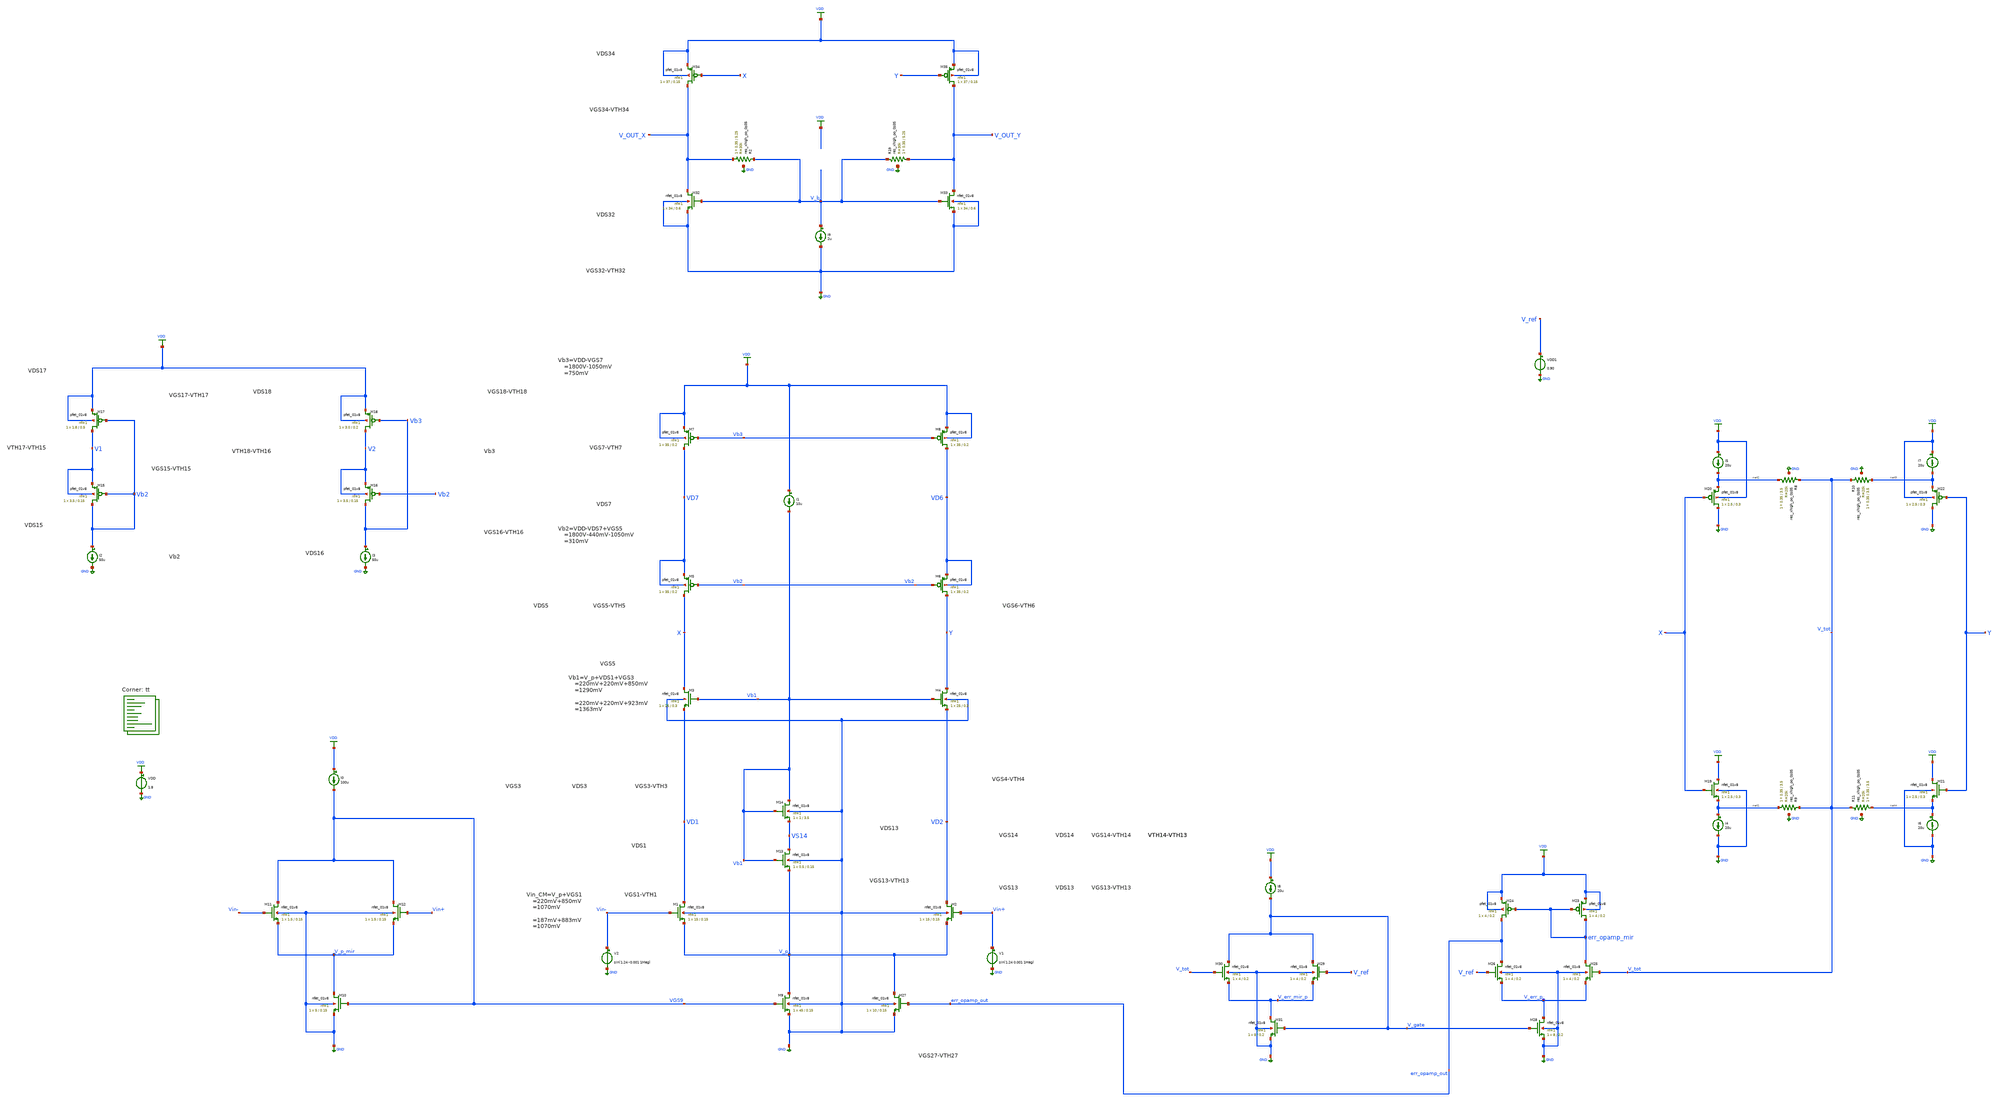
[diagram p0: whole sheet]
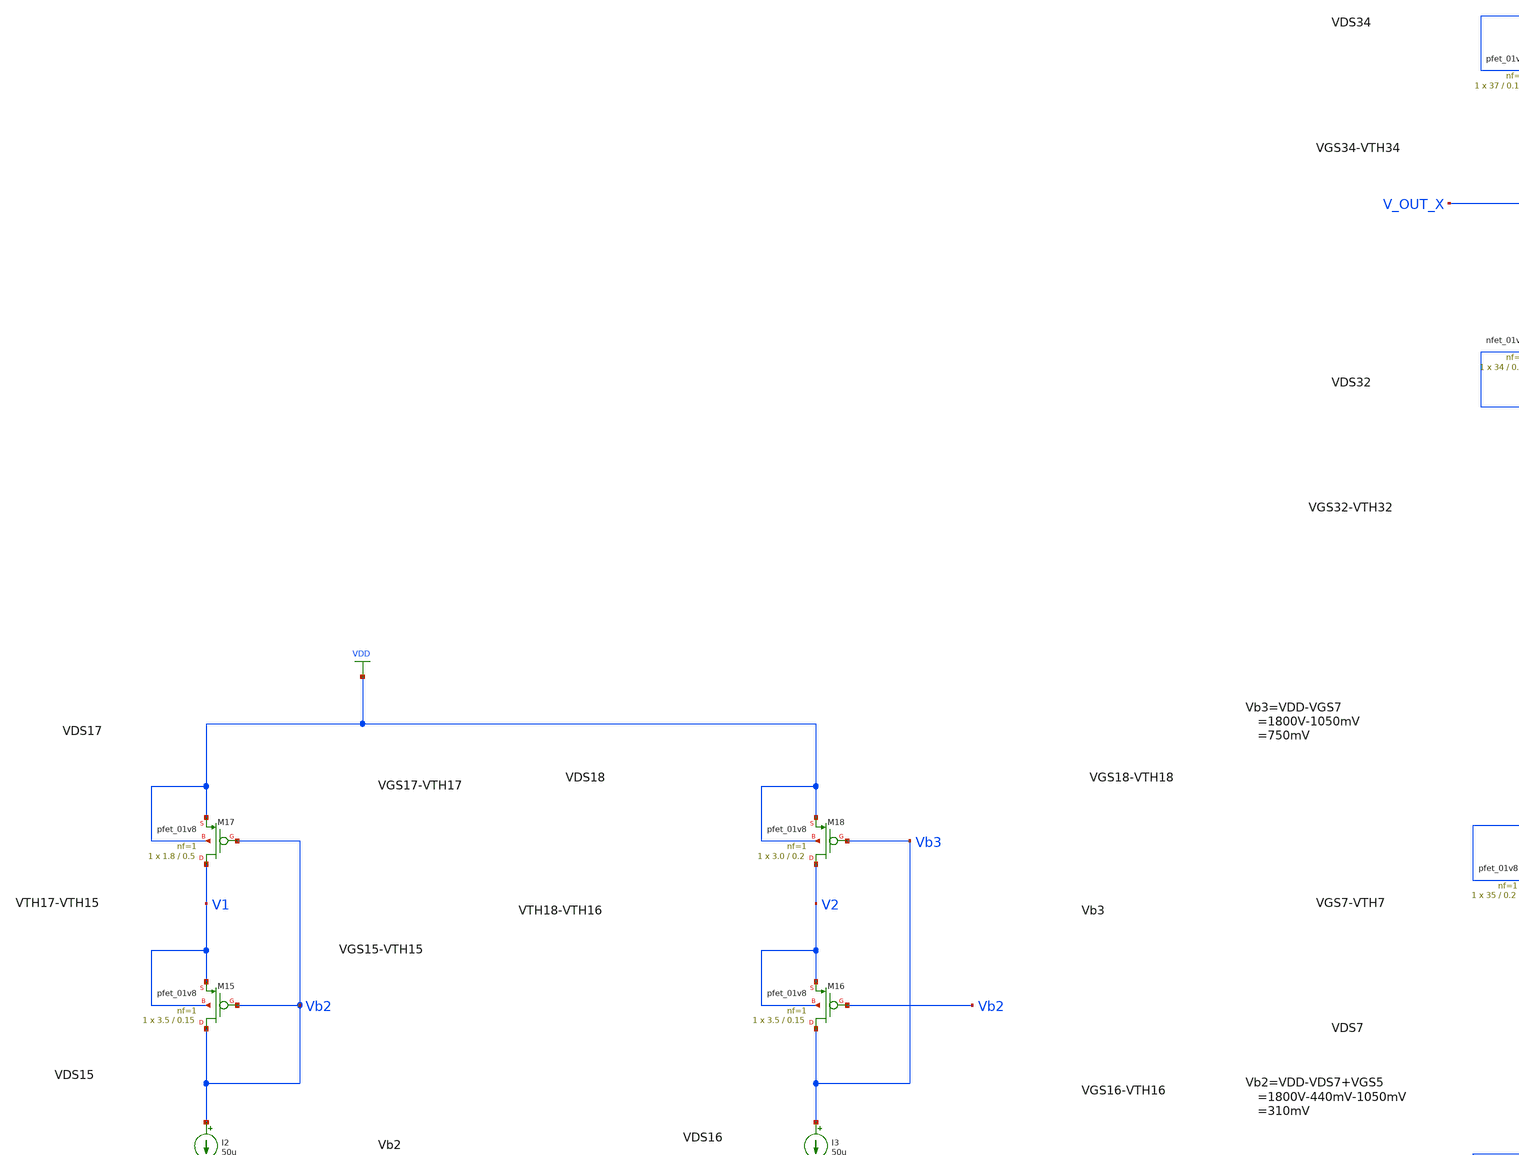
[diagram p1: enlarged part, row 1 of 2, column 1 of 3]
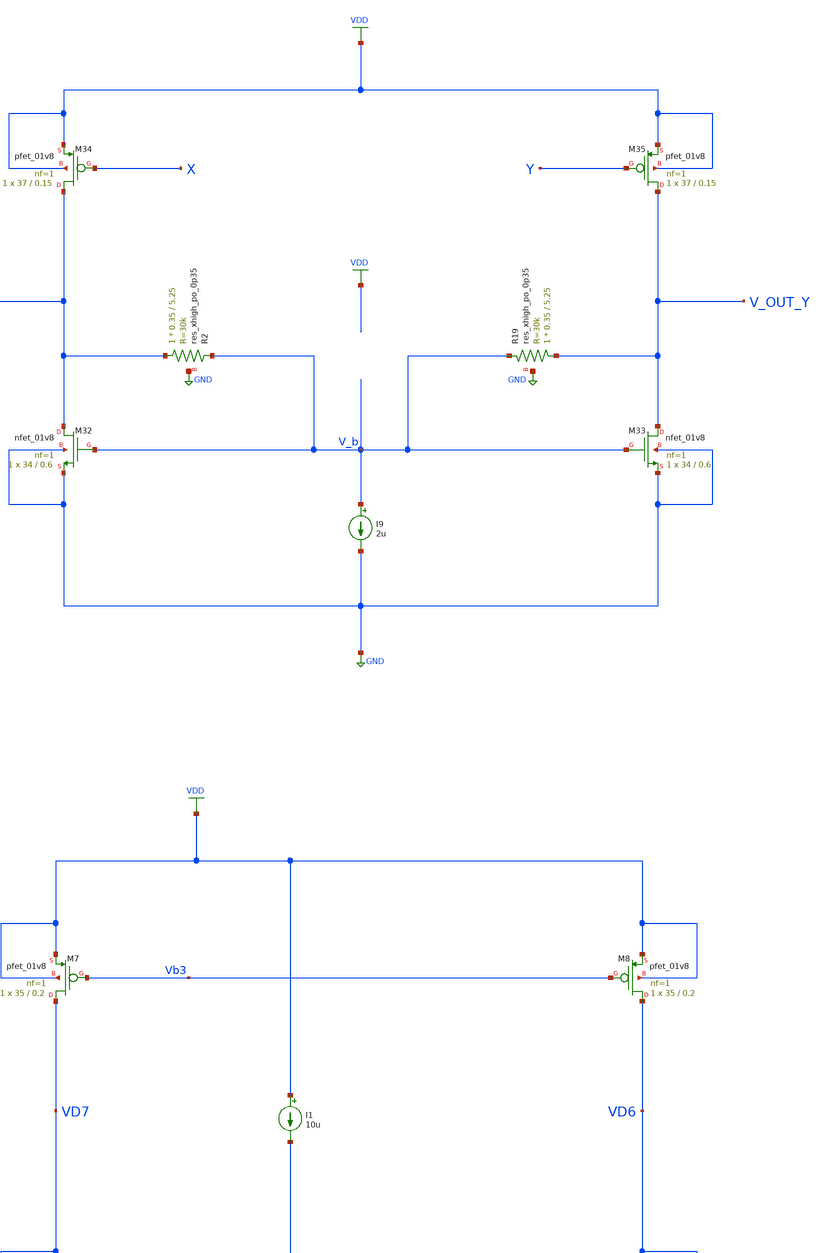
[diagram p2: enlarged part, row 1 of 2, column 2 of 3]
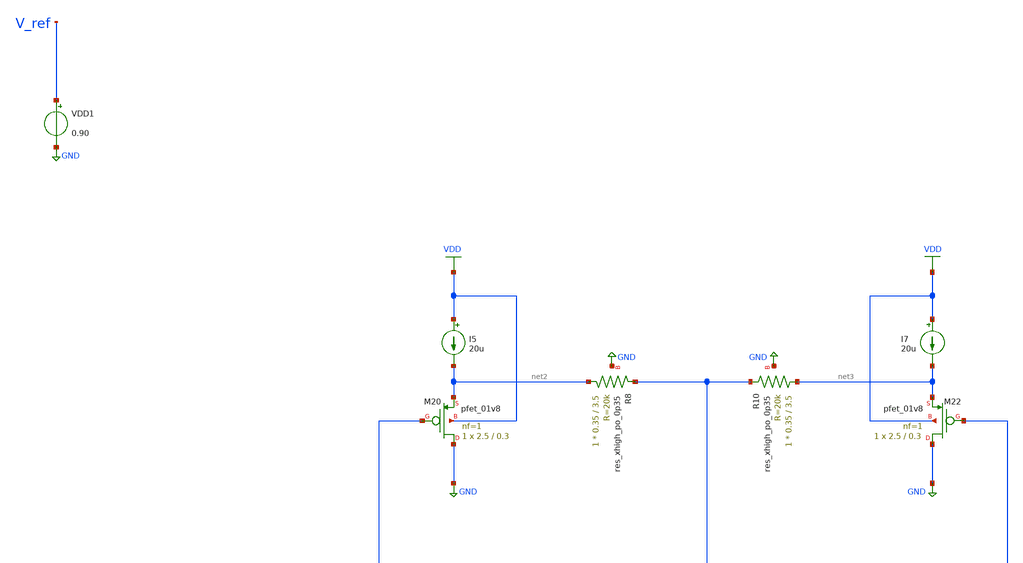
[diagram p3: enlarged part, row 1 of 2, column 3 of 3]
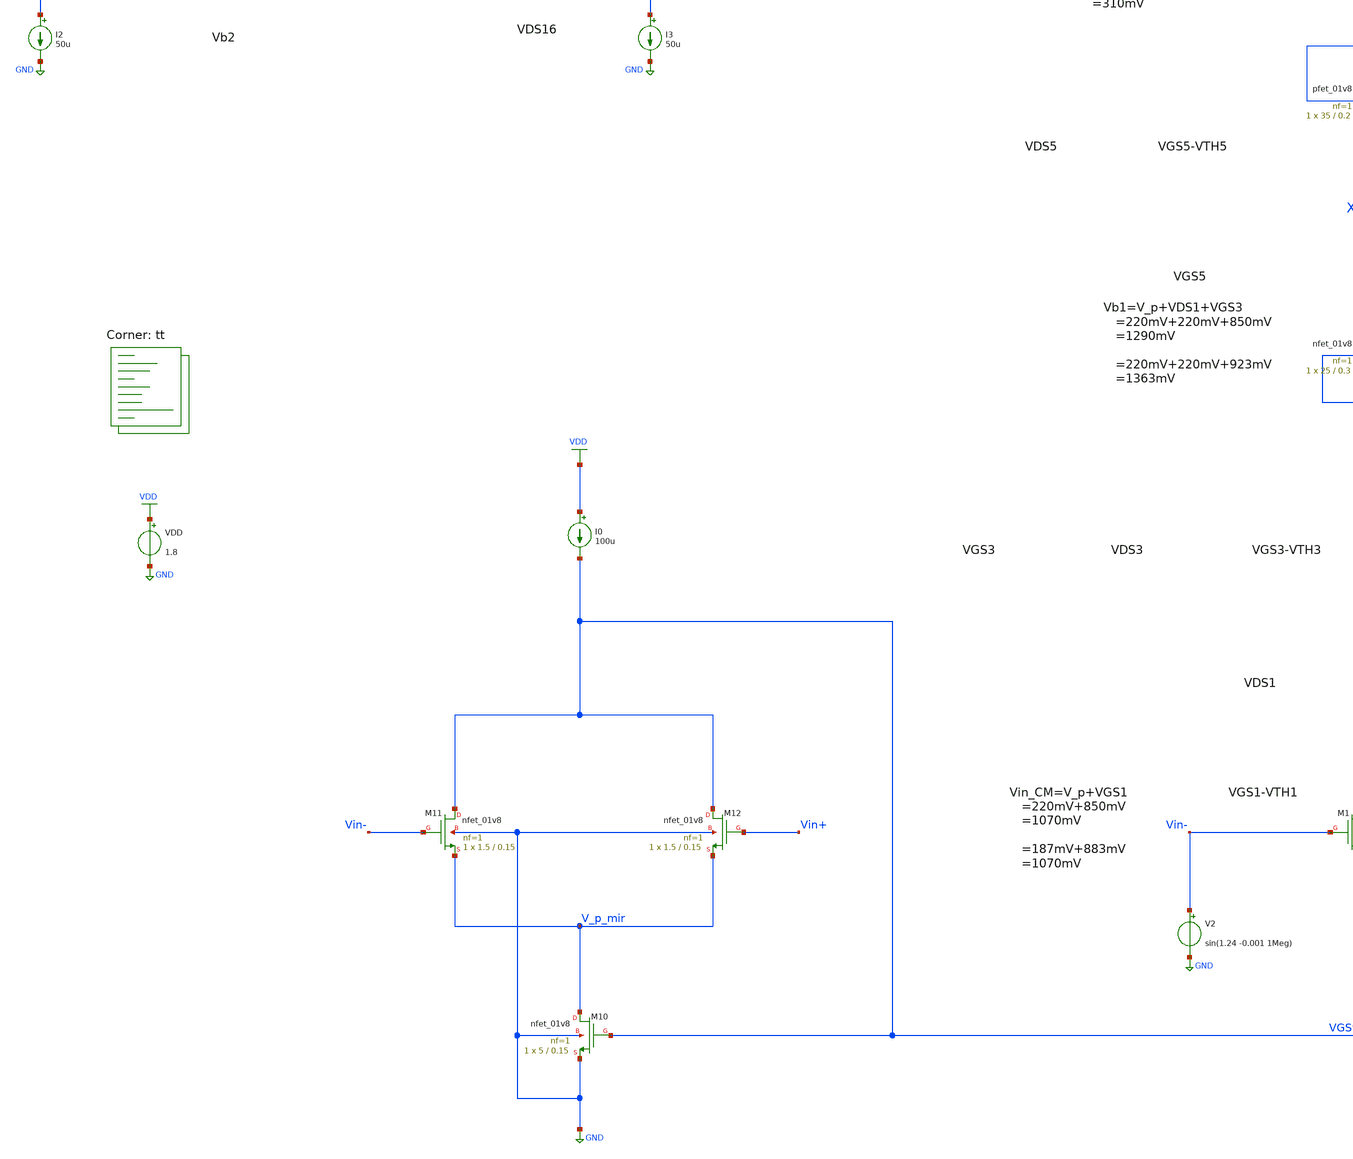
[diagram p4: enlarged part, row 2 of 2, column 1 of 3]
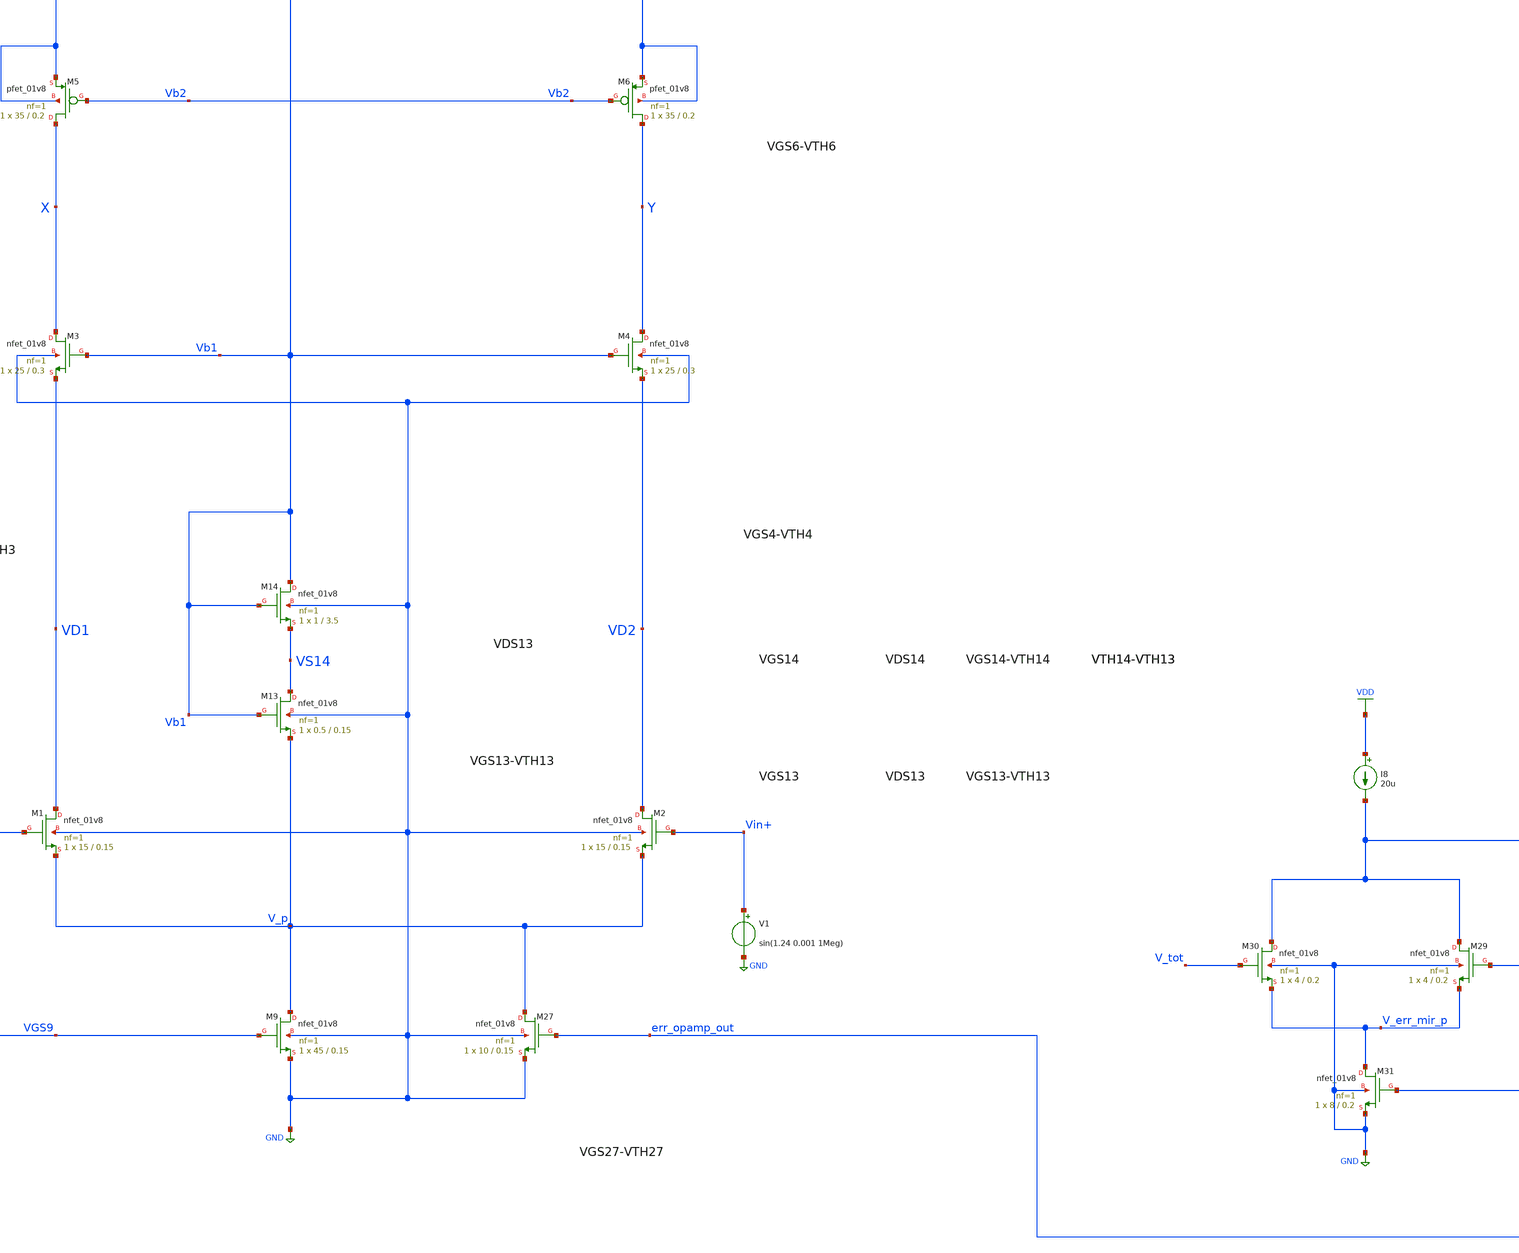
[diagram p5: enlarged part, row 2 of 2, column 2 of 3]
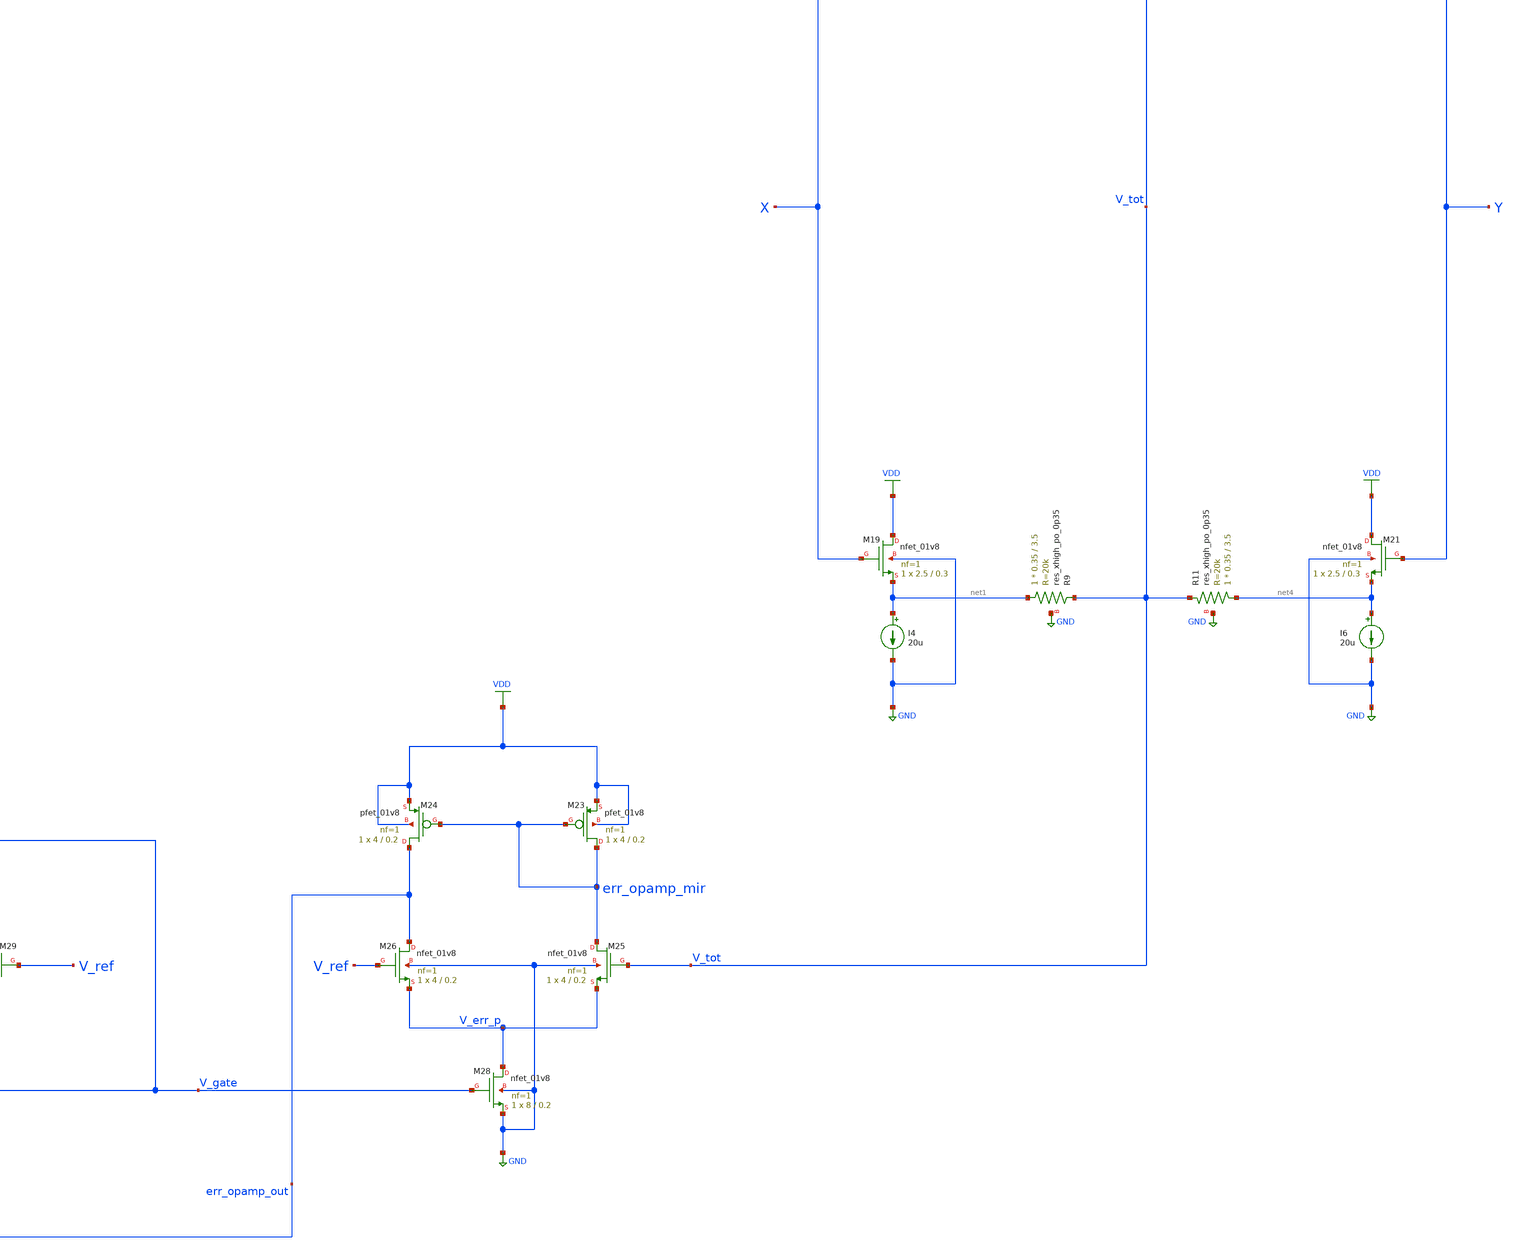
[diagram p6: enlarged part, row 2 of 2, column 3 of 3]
** sch_path: projects/opamp/xschem_ngspice/tb_opamp_1st_stage_3.sch
**.subckt tb_opamp_1st_stage_3
VDD VDD GND 1.8
XM1 VD1 Vin- V_p GND sky130_fd_pr__nfet_01v8 L=0.15 W=15 nf=1 ad='int((nf+1)/2) * W/nf * 0.29' as='int((nf+2)/2) * W/nf * 0.29'
+ pd='2*int((nf+1)/2) * (W/nf + 0.29)' ps='2*int((nf+2)/2) * (W/nf + 0.29)' nrd='0.29 / W' nrs='0.29 / W'
+ sa=0 sb=0 sd=0 mult=1 m=1
XM2 VD2 Vin+ V_p GND sky130_fd_pr__nfet_01v8 L=0.15 W=15 nf=1 ad='int((nf+1)/2) * W/nf * 0.29' as='int((nf+2)/2) * W/nf * 0.29'
+ pd='2*int((nf+1)/2) * (W/nf + 0.29)' ps='2*int((nf+2)/2) * (W/nf + 0.29)' nrd='0.29 / W' nrs='0.29 / W'
+ sa=0 sb=0 sd=0 mult=1 m=1
XM3 X Vb1 VD1 GND sky130_fd_pr__nfet_01v8 L=0.3 W=25 nf=1 ad='int((nf+1)/2) * W/nf * 0.29' as='int((nf+2)/2) * W/nf * 0.29'
+ pd='2*int((nf+1)/2) * (W/nf + 0.29)' ps='2*int((nf+2)/2) * (W/nf + 0.29)' nrd='0.29 / W' nrs='0.29 / W'
+ sa=0 sb=0 sd=0 mult=1 m=1
XM4 Y Vb1 VD2 GND sky130_fd_pr__nfet_01v8 L=0.3 W=25 nf=1 ad='int((nf+1)/2) * W/nf * 0.29' as='int((nf+2)/2) * W/nf * 0.29'
+ pd='2*int((nf+1)/2) * (W/nf + 0.29)' ps='2*int((nf+2)/2) * (W/nf + 0.29)' nrd='0.29 / W' nrs='0.29 / W'
+ sa=0 sb=0 sd=0 mult=1 m=1
XM5 X Vb2 VD7 VD7 sky130_fd_pr__pfet_01v8 L=0.2 W=35 nf=1 ad='int((nf+1)/2) * W/nf * 0.29' as='int((nf+2)/2) * W/nf * 0.29'
+ pd='2*int((nf+1)/2) * (W/nf + 0.29)' ps='2*int((nf+2)/2) * (W/nf + 0.29)' nrd='0.29 / W' nrs='0.29 / W'
+ sa=0 sb=0 sd=0 mult=1 m=1
XM6 Y Vb2 VD6 VD6 sky130_fd_pr__pfet_01v8 L=0.2 W=35 nf=1 ad='int((nf+1)/2) * W/nf * 0.29' as='int((nf+2)/2) * W/nf * 0.29'
+ pd='2*int((nf+1)/2) * (W/nf + 0.29)' ps='2*int((nf+2)/2) * (W/nf + 0.29)' nrd='0.29 / W' nrs='0.29 / W'
+ sa=0 sb=0 sd=0 mult=1 m=1
XM7 VD7 Vb3 VDD VDD sky130_fd_pr__pfet_01v8 L=0.2 W=35 nf=1 ad='int((nf+1)/2) * W/nf * 0.29' as='int((nf+2)/2) * W/nf * 0.29'
+ pd='2*int((nf+1)/2) * (W/nf + 0.29)' ps='2*int((nf+2)/2) * (W/nf + 0.29)' nrd='0.29 / W' nrs='0.29 / W'
+ sa=0 sb=0 sd=0 mult=1 m=1
XM8 VD6 Vb3 VDD VDD sky130_fd_pr__pfet_01v8 L=0.2 W=35 nf=1 ad='int((nf+1)/2) * W/nf * 0.29' as='int((nf+2)/2) * W/nf * 0.29'
+ pd='2*int((nf+1)/2) * (W/nf + 0.29)' ps='2*int((nf+2)/2) * (W/nf + 0.29)' nrd='0.29 / W' nrs='0.29 / W'
+ sa=0 sb=0 sd=0 mult=1 m=1
XM9 V_p VGS9 GND GND sky130_fd_pr__nfet_01v8 L=0.15 W=45 nf=1 ad='int((nf+1)/2) * W/nf * 0.29' as='int((nf+2)/2) * W/nf * 0.29'
+ pd='2*int((nf+1)/2) * (W/nf + 0.29)' ps='2*int((nf+2)/2) * (W/nf + 0.29)' nrd='0.29 / W' nrs='0.29 / W'
+ sa=0 sb=0 sd=0 mult=1 m=1
XM10 V_p_mir VGS9 GND GND sky130_fd_pr__nfet_01v8 L=0.15 W=5 nf=1 ad='int((nf+1)/2) * W/nf * 0.29' as='int((nf+2)/2) * W/nf * 0.29'
+ pd='2*int((nf+1)/2) * (W/nf + 0.29)' ps='2*int((nf+2)/2) * (W/nf + 0.29)' nrd='0.29 / W' nrs='0.29 / W'
+ sa=0 sb=0 sd=0 mult=1 m=1
I0 VDD VGS9 100u
XM11 VGS9 Vin- V_p_mir GND sky130_fd_pr__nfet_01v8 L=0.15 W=1.5 nf=1 ad='int((nf+1)/2) * W/nf * 0.29'
+ as='int((nf+2)/2) * W/nf * 0.29' pd='2*int((nf+1)/2) * (W/nf + 0.29)' ps='2*int((nf+2)/2) * (W/nf + 0.29)'
+ nrd='0.29 / W' nrs='0.29 / W' sa=0 sb=0 sd=0 mult=1 m=1
XM12 VGS9 Vin+ V_p_mir GND sky130_fd_pr__nfet_01v8 L=0.15 W=1.5 nf=1 ad='int((nf+1)/2) * W/nf * 0.29'
+ as='int((nf+2)/2) * W/nf * 0.29' pd='2*int((nf+1)/2) * (W/nf + 0.29)' ps='2*int((nf+2)/2) * (W/nf + 0.29)'
+ nrd='0.29 / W' nrs='0.29 / W' sa=0 sb=0 sd=0 mult=1 m=1
XM13 VS14 Vb1 V_p GND sky130_fd_pr__nfet_01v8 L=0.15 W=0.5 nf=1 ad='int((nf+1)/2) * W/nf * 0.29' as='int((nf+2)/2) * W/nf * 0.29'
+ pd='2*int((nf+1)/2) * (W/nf + 0.29)' ps='2*int((nf+2)/2) * (W/nf + 0.29)' nrd='0.29 / W' nrs='0.29 / W'
+ sa=0 sb=0 sd=0 mult=1 m=1
XM14 Vb1 Vb1 VS14 GND sky130_fd_pr__nfet_01v8 L=3.5 W=1 nf=1 ad='int((nf+1)/2) * W/nf * 0.29' as='int((nf+2)/2) * W/nf * 0.29'
+ pd='2*int((nf+1)/2) * (W/nf + 0.29)' ps='2*int((nf+2)/2) * (W/nf + 0.29)' nrd='0.29 / W' nrs='0.29 / W'
+ sa=0 sb=0 sd=0 mult=1 m=1
I1 VDD Vb1 10u
XM15 Vb2 Vb2 V1 V1 sky130_fd_pr__pfet_01v8 L=0.15 W=3.5 nf=1 ad='int((nf+1)/2) * W/nf * 0.29' as='int((nf+2)/2) * W/nf * 0.29'
+ pd='2*int((nf+1)/2) * (W/nf + 0.29)' ps='2*int((nf+2)/2) * (W/nf + 0.29)' nrd='0.29 / W' nrs='0.29 / W'
+ sa=0 sb=0 sd=0 mult=1 m=1
XM16 Vb3 Vb2 V2 V2 sky130_fd_pr__pfet_01v8 L=0.15 W=3.5 nf=1 ad='int((nf+1)/2) * W/nf * 0.29' as='int((nf+2)/2) * W/nf * 0.29'
+ pd='2*int((nf+1)/2) * (W/nf + 0.29)' ps='2*int((nf+2)/2) * (W/nf + 0.29)' nrd='0.29 / W' nrs='0.29 / W'
+ sa=0 sb=0 sd=0 mult=1 m=1
XM17 V1 Vb2 VDD VDD sky130_fd_pr__pfet_01v8 L=0.5 W=1.8 nf=1 ad='int((nf+1)/2) * W/nf * 0.29' as='int((nf+2)/2) * W/nf * 0.29'
+ pd='2*int((nf+1)/2) * (W/nf + 0.29)' ps='2*int((nf+2)/2) * (W/nf + 0.29)' nrd='0.29 / W' nrs='0.29 / W'
+ sa=0 sb=0 sd=0 mult=1 m=1
XM18 V2 Vb3 VDD VDD sky130_fd_pr__pfet_01v8 L=0.2 W=3.0 nf=1 ad='int((nf+1)/2) * W/nf * 0.29' as='int((nf+2)/2) * W/nf * 0.29'
+ pd='2*int((nf+1)/2) * (W/nf + 0.29)' ps='2*int((nf+2)/2) * (W/nf + 0.29)' nrd='0.29 / W' nrs='0.29 / W'
+ sa=0 sb=0 sd=0 mult=1 m=1
I2 Vb2 GND 50u
I3 Vb3 GND 50u
XM19 VDD X net1 GND sky130_fd_pr__nfet_01v8 L=0.3 W=2.5 nf=1 ad='int((nf+1)/2) * W/nf * 0.29' as='int((nf+2)/2) * W/nf * 0.29'
+ pd='2*int((nf+1)/2) * (W/nf + 0.29)' ps='2*int((nf+2)/2) * (W/nf + 0.29)' nrd='0.29 / W' nrs='0.29 / W'
+ sa=0 sb=0 sd=0 mult=1 m=1
XM20 GND X net2 VDD sky130_fd_pr__pfet_01v8 L=0.3 W=2.5 nf=1 ad='int((nf+1)/2) * W/nf * 0.29' as='int((nf+2)/2) * W/nf * 0.29'
+ pd='2*int((nf+1)/2) * (W/nf + 0.29)' ps='2*int((nf+2)/2) * (W/nf + 0.29)' nrd='0.29 / W' nrs='0.29 / W'
+ sa=0 sb=0 sd=0 mult=1 m=1
I4 net1 GND 20u
I5 VDD net2 20u
XR8 net2 V_tot GND sky130_fd_pr__res_xhigh_po_0p35 L=3.5 mult=1 m=1
XR9 net1 V_tot GND sky130_fd_pr__res_xhigh_po_0p35 L=3.5 mult=1 m=1
XR10 net3 V_tot GND sky130_fd_pr__res_xhigh_po_0p35 L=3.5 mult=1 m=1
XR11 net4 V_tot GND sky130_fd_pr__res_xhigh_po_0p35 L=3.5 mult=1 m=1
XM21 VDD Y net4 GND sky130_fd_pr__nfet_01v8 L=0.3 W=2.5 nf=1 ad='int((nf+1)/2) * W/nf * 0.29' as='int((nf+2)/2) * W/nf * 0.29'
+ pd='2*int((nf+1)/2) * (W/nf + 0.29)' ps='2*int((nf+2)/2) * (W/nf + 0.29)' nrd='0.29 / W' nrs='0.29 / W'
+ sa=0 sb=0 sd=0 mult=1 m=1
XM22 GND Y net3 VDD sky130_fd_pr__pfet_01v8 L=0.3 W=2.5 nf=1 ad='int((nf+1)/2) * W/nf * 0.29' as='int((nf+2)/2) * W/nf * 0.29'
+ pd='2*int((nf+1)/2) * (W/nf + 0.29)' ps='2*int((nf+2)/2) * (W/nf + 0.29)' nrd='0.29 / W' nrs='0.29 / W'
+ sa=0 sb=0 sd=0 mult=1 m=1
I6 net4 GND 20u
I7 VDD net3 20u
VDD1 V_ref GND 0.90
V2 Vin- GND sin(1.24 -0.001 1Meg)
V1 Vin+ GND sin(1.24 0.001 1Meg)
XM32 V_OUT_X V_b GND GND sky130_fd_pr__nfet_01v8 L=0.6 W=34 nf=1 ad='int((nf+1)/2) * W/nf * 0.29' as='int((nf+2)/2) * W/nf * 0.29'
+ pd='2*int((nf+1)/2) * (W/nf + 0.29)' ps='2*int((nf+2)/2) * (W/nf + 0.29)' nrd='0.29 / W' nrs='0.29 / W'
+ sa=0 sb=0 sd=0 mult=1 m=1
XM33 V_OUT_Y V_b GND GND sky130_fd_pr__nfet_01v8 L=0.6 W=34 nf=1 ad='int((nf+1)/2) * W/nf * 0.29' as='int((nf+2)/2) * W/nf * 0.29'
+ pd='2*int((nf+1)/2) * (W/nf + 0.29)' ps='2*int((nf+2)/2) * (W/nf + 0.29)' nrd='0.29 / W' nrs='0.29 / W'
+ sa=0 sb=0 sd=0 mult=1 m=1
XM34 V_OUT_X X VDD VDD sky130_fd_pr__pfet_01v8 L=0.15 W=37 nf=1 ad='int((nf+1)/2) * W/nf * 0.29' as='int((nf+2)/2) * W/nf * 0.29'
+ pd='2*int((nf+1)/2) * (W/nf + 0.29)' ps='2*int((nf+2)/2) * (W/nf + 0.29)' nrd='0.29 / W' nrs='0.29 / W'
+ sa=0 sb=0 sd=0 mult=1 m=1
XM35 V_OUT_Y Y VDD VDD sky130_fd_pr__pfet_01v8 L=0.15 W=37 nf=1 ad='int((nf+1)/2) * W/nf * 0.29' as='int((nf+2)/2) * W/nf * 0.29'
+ pd='2*int((nf+1)/2) * (W/nf + 0.29)' ps='2*int((nf+2)/2) * (W/nf + 0.29)' nrd='0.29 / W' nrs='0.29 / W'
+ sa=0 sb=0 sd=0 mult=1 m=1
XR2 V_OUT_X V_b GND sky130_fd_pr__res_xhigh_po_0p35 L=5.25 mult=1 m=1
XR19 V_OUT_Y V_b GND sky130_fd_pr__res_xhigh_po_0p35 L=5.25 mult=1 m=1
I9 V_b GND 2u
XM27 V_p err_opamp_out GND GND sky130_fd_pr__nfet_01v8 L=0.15 W=10 nf=1 ad='int((nf+1)/2) * W/nf * 0.29'
+ as='int((nf+2)/2) * W/nf * 0.29' pd='2*int((nf+1)/2) * (W/nf + 0.29)' ps='2*int((nf+2)/2) * (W/nf + 0.29)'
+ nrd='0.29 / W' nrs='0.29 / W' sa=0 sb=0 sd=0 mult=1 m=1
XM23 err_opamp_mir err_opamp_mir VDD VDD sky130_fd_pr__pfet_01v8 L=0.2 W=4 nf=1 ad='int((nf+1)/2) * W/nf * 0.29'
+ as='int((nf+2)/2) * W/nf * 0.29' pd='2*int((nf+1)/2) * (W/nf + 0.29)' ps='2*int((nf+2)/2) * (W/nf + 0.29)'
+ nrd='0.29 / W' nrs='0.29 / W' sa=0 sb=0 sd=0 mult=1 m=1
XM24 err_opamp_out err_opamp_mir VDD VDD sky130_fd_pr__pfet_01v8 L=0.2 W=4 nf=1 ad='int((nf+1)/2) * W/nf * 0.29'
+ as='int((nf+2)/2) * W/nf * 0.29' pd='2*int((nf+1)/2) * (W/nf + 0.29)' ps='2*int((nf+2)/2) * (W/nf + 0.29)'
+ nrd='0.29 / W' nrs='0.29 / W' sa=0 sb=0 sd=0 mult=1 m=1
I8 VDD V_gate 20u
XM25 err_opamp_mir V_tot V_err_p GND sky130_fd_pr__nfet_01v8 L=0.2 W=4 nf=1 ad='int((nf+1)/2) * W/nf * 0.29'
+ as='int((nf+2)/2) * W/nf * 0.29' pd='2*int((nf+1)/2) * (W/nf + 0.29)' ps='2*int((nf+2)/2) * (W/nf + 0.29)'
+ nrd='0.29 / W' nrs='0.29 / W' sa=0 sb=0 sd=0 mult=1 m=1
XM26 err_opamp_out V_ref V_err_p GND sky130_fd_pr__nfet_01v8 L=0.2 W=4 nf=1 ad='int((nf+1)/2) * W/nf * 0.29'
+ as='int((nf+2)/2) * W/nf * 0.29' pd='2*int((nf+1)/2) * (W/nf + 0.29)' ps='2*int((nf+2)/2) * (W/nf + 0.29)'
+ nrd='0.29 / W' nrs='0.29 / W' sa=0 sb=0 sd=0 mult=1 m=1
XM28 V_err_p V_gate GND GND sky130_fd_pr__nfet_01v8 L=0.2 W=8 nf=1 ad='int((nf+1)/2) * W/nf * 0.29' as='int((nf+2)/2) * W/nf * 0.29'
+ pd='2*int((nf+1)/2) * (W/nf + 0.29)' ps='2*int((nf+2)/2) * (W/nf + 0.29)' nrd='0.29 / W' nrs='0.29 / W'
+ sa=0 sb=0 sd=0 mult=1 m=1
XM29 V_gate V_ref V_err_mir_p GND sky130_fd_pr__nfet_01v8 L=0.2 W=4 nf=1 ad='int((nf+1)/2) * W/nf * 0.29'
+ as='int((nf+2)/2) * W/nf * 0.29' pd='2*int((nf+1)/2) * (W/nf + 0.29)' ps='2*int((nf+2)/2) * (W/nf + 0.29)'
+ nrd='0.29 / W' nrs='0.29 / W' sa=0 sb=0 sd=0 mult=1 m=1
XM30 V_gate V_tot V_err_mir_p GND sky130_fd_pr__nfet_01v8 L=0.2 W=4 nf=1 ad='int((nf+1)/2) * W/nf * 0.29'
+ as='int((nf+2)/2) * W/nf * 0.29' pd='2*int((nf+1)/2) * (W/nf + 0.29)' ps='2*int((nf+2)/2) * (W/nf + 0.29)'
+ nrd='0.29 / W' nrs='0.29 / W' sa=0 sb=0 sd=0 mult=1 m=1
XM31 V_err_mir_p V_gate GND GND sky130_fd_pr__nfet_01v8 L=0.2 W=8 nf=1 ad='int((nf+1)/2) * W/nf * 0.29'
+ as='int((nf+2)/2) * W/nf * 0.29' pd='2*int((nf+1)/2) * (W/nf + 0.29)' ps='2*int((nf+2)/2) * (W/nf + 0.29)'
+ nrd='0.29 / W' nrs='0.29 / W' sa=0 sb=0 sd=0 mult=1 m=1
**** begin user architecture code



.option method=gear
.option wnflag=1
.option savecurrents

.save @m.xm1.msky130_fd_pr__nfet_01v8[gm] @m.xm1.msky130_fd_pr__nfet_01v8[vth] @m.xm2.msky130_fd_pr__nfet_01v8[gm] @m.xm2.msky130_fd_pr__nfet_01v8[vth] @m.xm3.msky130_fd_pr__nfet_01v8[gm] @m.xm3.msky130_fd_pr__nfet_01v8[vth] @m.xm4.msky130_fd_pr__nfet_01v8[gm] @m.xm4.msky130_fd_pr__nfet_01v8[vth] @m.xm5.msky130_fd_pr__pfet_01v8[gm] @m.xm5.msky130_fd_pr__pfet_01v8[vth] @m.xm6.msky130_fd_pr__pfet_01v8[gm] @m.xm6.msky130_fd_pr__pfet_01v8[vth] @m.xm7.msky130_fd_pr__pfet_01v8[gm] @m.xm7.msky130_fd_pr__pfet_01v8[vth] @m.xm8.msky130_fd_pr__pfet_01v8[gm] @m.xm8.msky130_fd_pr__pfet_01v8[vth] @m.xm9.msky130_fd_pr__nfet_01v8[gm] @m.xm9.msky130_fd_pr__nfet_01v8[vth] @m.xm10.msky130_fd_pr__nfet_01v8[gm] @m.xm10.msky130_fd_pr__nfet_01v8[vth] @m.xm11.msky130_fd_pr__nfet_01v8[gm] @m.xm11.msky130_fd_pr__nfet_01v8[vth] @m.xm12.msky130_fd_pr__nfet_01v8[gm] @m.xm12.msky130_fd_pr__nfet_01v8[vth] @m.xm13.msky130_fd_pr__nfet_01v8[gm] @m.xm13.msky130_fd_pr__nfet_01v8[vth] @m.xm14.msky130_fd_pr__nfet_01v8[gm] @m.xm14.msky130_fd_pr__nfet_01v8[vth] @m.xm15.msky130_fd_pr__pfet_01v8[gm] @m.xm15.msky130_fd_pr__pfet_01v8[vth] @m.xm16.msky130_fd_pr__pfet_01v8[gm] @m.xm16.msky130_fd_pr__pfet_01v8[vth] @m.xm17.msky130_fd_pr__pfet_01v8[gm] @m.xm17.msky130_fd_pr__pfet_01v8[vth] @m.xm18.msky130_fd_pr__pfet_01v8[gm] @m.xm18.msky130_fd_pr__pfet_01v8[vth] @m.xm19.msky130_fd_pr__nfet_01v8[gm] @m.xm19.msky130_fd_pr__nfet_01v8[vth] @m.xm20.msky130_fd_pr__pfet_01v8[gm] @m.xm20.msky130_fd_pr__pfet_01v8[vth] @m.xm21.msky130_fd_pr__nfet_01v8[gm] @m.xm21.msky130_fd_pr__nfet_01v8[vth] @m.xm22.msky130_fd_pr__pfet_01v8[gm] @m.xm22.msky130_fd_pr__pfet_01v8[vth] @m.xm23.msky130_fd_pr__pfet_01v8[gm] @m.xm23.msky130_fd_pr__pfet_01v8[vth] @m.xm24.msky130_fd_pr__pfet_01v8[gm] @m.xm24.msky130_fd_pr__pfet_01v8[vth] @m.xm25.msky130_fd_pr__nfet_01v8[gm] @m.xm25.msky130_fd_pr__nfet_01v8[vth] @m.xm26.msky130_fd_pr__nfet_01v8[gm] @m.xm26.msky130_fd_pr__nfet_01v8[vth] @m.xm27.msky130_fd_pr__nfet_01v8[gm] @m.xm27.msky130_fd_pr__nfet_01v8[vth] @m.xm28.msky130_fd_pr__nfet_01v8[gm] @m.xm28.msky130_fd_pr__nfet_01v8[vth] @m.xm29.msky130_fd_pr__nfet_01v8[gm] @m.xm29.msky130_fd_pr__nfet_01v8[vth] @m.xm30.msky130_fd_pr__nfet_01v8[gm] @m.xm30.msky130_fd_pr__nfet_01v8[vth] @m.xm31.msky130_fd_pr__nfet_01v8[gm] @m.xm31.msky130_fd_pr__nfet_01v8[vth] @m.xm32.msky130_fd_pr__nfet_01v8[gm] @m.xm32.msky130_fd_pr__nfet_01v8[vth] @m.xm33.msky130_fd_pr__nfet_01v8[gm] @m.xm33.msky130_fd_pr__nfet_01v8[vth] @m.xm34.msky130_fd_pr__pfet_01v8[gm] @m.xm34.msky130_fd_pr__pfet_01v8[vth] @m.xm35.msky130_fd_pr__pfet_01v8[gm] @m.xm35.msky130_fd_pr__pfet_01v8[vth]


.control

  save all
  * dc VDD 0 1.8 0.9
  * tran 0.4u 3m
  tran 0.4n 3u
  * ac dec 20 1 1T
  remzerovec
  write tb_opamp_1st_stage_3.raw
  set appendwrite
  let first_out = x - y
  let second_out = v_out_x - v_out_y

.endc




.lib $::SKYWATER_MODELS/sky130.lib.spice tt
**** end user architecture code
**.ends
.GLOBAL GND
.GLOBAL VDD
.end
